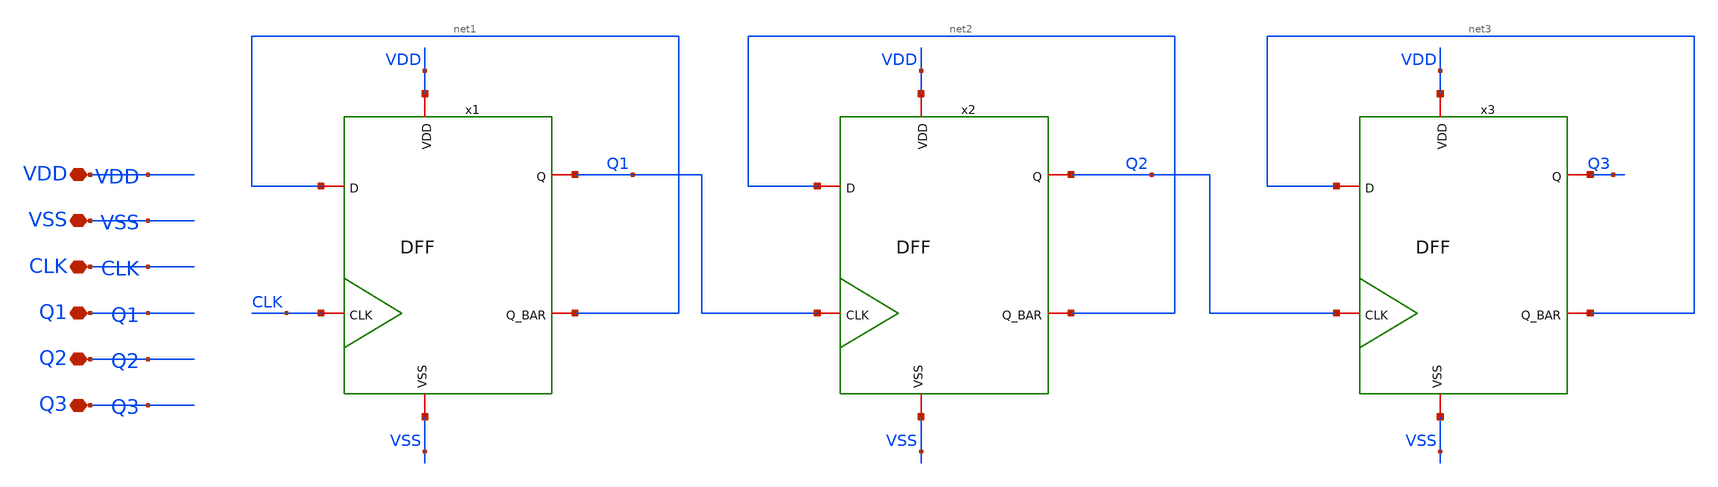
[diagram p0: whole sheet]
** sch_path: designs/libs/xp_core_analog/xp_DIV8/DIVD8.sch
**.subckt DIVD8 VDD VSS CLK Q1 Q2 Q3
*.iopin VDD
*.iopin VSS
*.iopin CLK
*.iopin Q1
*.iopin Q2
*.iopin Q3
x1 VDD VSS CLK net1 Q1 net1 DFF
x2 VDD VSS Q1 net2 Q2 net2 DFF
x3 VDD VSS Q2 net3 Q3 net3 DFF
**.ends

* expanding   symbol:  libs/core_analog/xp_DFF/DFF.sym # of pins=6
** sym_path: designs/libs/core_analog/xp_DFF/DFF.sym
** sch_path: designs/libs/core_analog/xp_DFF/DFF.sch
.subckt DFF VDD VSS CLK D Q Q_BAR
*.iopin VDD
*.iopin VSS
*.iopin CLK
*.iopin D
*.iopin Q_BAR
*.iopin Q
XM1 CLK_B CLK VSS VSS nfet_03v3 L=0.28u W=0.5u nf=1 ad='int((nf+1)/2) * W/nf * 0.18u' as='int((nf+2)/2) * W/nf * 0.18u'
+ pd='2*int((nf+1)/2) * (W/nf + 0.18u)' ps='2*int((nf+2)/2) * (W/nf + 0.18u)' nrd='0.18u / W' nrs='0.18u / W'
+ sa=0 sb=0 sd=0 m=1
XM2 CLK_B CLK VDD VDD pfet_03v3 L=0.28u W=1u nf=1 ad='int((nf+1)/2) * W/nf * 0.18u' as='int((nf+2)/2) * W/nf * 0.18u'
+ pd='2*int((nf+1)/2) * (W/nf + 0.18u)' ps='2*int((nf+2)/2) * (W/nf + 0.18u)' nrd='0.18u / W' nrs='0.18u / W'
+ sa=0 sb=0 sd=0 m=1
XM3 net1 D net3 VSS nfet_03v3 L=0.28u W=0.5u nf=1 ad='int((nf+1)/2) * W/nf * 0.18u' as='int((nf+2)/2) * W/nf * 0.18u'
+ pd='2*int((nf+1)/2) * (W/nf + 0.18u)' ps='2*int((nf+2)/2) * (W/nf + 0.18u)' nrd='0.18u / W' nrs='0.18u / W'
+ sa=0 sb=0 sd=0 m=1
XM4 net1 D net2 VDD pfet_03v3 L=0.28u W=1u nf=1 ad='int((nf+1)/2) * W/nf * 0.18u' as='int((nf+2)/2) * W/nf * 0.18u'
+ pd='2*int((nf+1)/2) * (W/nf + 0.18u)' ps='2*int((nf+2)/2) * (W/nf + 0.18u)' nrd='0.18u / W' nrs='0.18u / W'
+ sa=0 sb=0 sd=0 m=1
XM5 net2 CLK VDD VDD pfet_03v3 L=0.28u W=1u nf=1 ad='int((nf+1)/2) * W/nf * 0.18u' as='int((nf+2)/2) * W/nf * 0.18u'
+ pd='2*int((nf+1)/2) * (W/nf + 0.18u)' ps='2*int((nf+2)/2) * (W/nf + 0.18u)' nrd='0.18u / W' nrs='0.18u / W'
+ sa=0 sb=0 sd=0 m=1
XM6 net3 CLK_B VSS VSS nfet_03v3 L=0.28u W=0.5u nf=1 ad='int((nf+1)/2) * W/nf * 0.18u' as='int((nf+2)/2) * W/nf * 0.18u'
+ pd='2*int((nf+1)/2) * (W/nf + 0.18u)' ps='2*int((nf+2)/2) * (W/nf + 0.18u)' nrd='0.18u / W' nrs='0.18u / W'
+ sa=0 sb=0 sd=0 m=1
XM7 net1 CLK_B net6 VSS nfet_03v3 L=0.28u W=0.22u nf=1 ad='int((nf+1)/2) * W/nf * 0.18u' as='int((nf+2)/2) * W/nf * 0.18u'
+ pd='2*int((nf+1)/2) * (W/nf + 0.18u)' ps='2*int((nf+2)/2) * (W/nf + 0.18u)' nrd='0.18u / W' nrs='0.18u / W'
+ sa=0 sb=0 sd=0 m=1
XM8 net1 CLK net4 VDD pfet_03v3 L=0.28u W=1u nf=1 ad='int((nf+1)/2) * W/nf * 0.18u' as='int((nf+2)/2) * W/nf * 0.18u'
+ pd='2*int((nf+1)/2) * (W/nf + 0.18u)' ps='2*int((nf+2)/2) * (W/nf + 0.18u)' nrd='0.18u / W' nrs='0.18u / W'
+ sa=0 sb=0 sd=0 m=1
XM9 net4 net5 VDD VDD pfet_03v3 L=0.28u W=1u nf=1 ad='int((nf+1)/2) * W/nf * 0.18u' as='int((nf+2)/2) * W/nf * 0.18u'
+ pd='2*int((nf+1)/2) * (W/nf + 0.18u)' ps='2*int((nf+2)/2) * (W/nf + 0.18u)' nrd='0.18u / W' nrs='0.18u / W'
+ sa=0 sb=0 sd=0 m=1
XM10 net6 net5 VSS VSS nfet_03v3 L=0.28u W=0.22u nf=1 ad='int((nf+1)/2) * W/nf * 0.18u' as='int((nf+2)/2) * W/nf * 0.18u'
+ pd='2*int((nf+1)/2) * (W/nf + 0.18u)' ps='2*int((nf+2)/2) * (W/nf + 0.18u)' nrd='0.18u / W' nrs='0.18u / W'
+ sa=0 sb=0 sd=0 m=1
XM11 net5 net1 VSS VSS nfet_03v3 L=0.28u W=0.5u nf=1 ad='int((nf+1)/2) * W/nf * 0.18u' as='int((nf+2)/2) * W/nf * 0.18u'
+ pd='2*int((nf+1)/2) * (W/nf + 0.18u)' ps='2*int((nf+2)/2) * (W/nf + 0.18u)' nrd='0.18u / W' nrs='0.18u / W'
+ sa=0 sb=0 sd=0 m=1
XM12 net5 net1 VDD VDD pfet_03v3 L=0.28u W=1u nf=1 ad='int((nf+1)/2) * W/nf * 0.18u' as='int((nf+2)/2) * W/nf * 0.18u'
+ pd='2*int((nf+1)/2) * (W/nf + 0.18u)' ps='2*int((nf+2)/2) * (W/nf + 0.18u)' nrd='0.18u / W' nrs='0.18u / W'
+ sa=0 sb=0 sd=0 m=1
XM13 net7 CLK net9 VSS nfet_03v3 L=0.28u W=0.5u nf=1 ad='int((nf+1)/2) * W/nf * 0.18u' as='int((nf+2)/2) * W/nf * 0.18u'
+ pd='2*int((nf+1)/2) * (W/nf + 0.18u)' ps='2*int((nf+2)/2) * (W/nf + 0.18u)' nrd='0.18u / W' nrs='0.18u / W'
+ sa=0 sb=0 sd=0 m=1
XM14 net7 CLK_B net8 VDD pfet_03v3 L=0.28u W=1u nf=1 ad='int((nf+1)/2) * W/nf * 0.18u' as='int((nf+2)/2) * W/nf * 0.18u'
+ pd='2*int((nf+1)/2) * (W/nf + 0.18u)' ps='2*int((nf+2)/2) * (W/nf + 0.18u)' nrd='0.18u / W' nrs='0.18u / W'
+ sa=0 sb=0 sd=0 m=1
XM15 net8 net5 VDD VDD pfet_03v3 L=0.28u W=1u nf=1 ad='int((nf+1)/2) * W/nf * 0.18u' as='int((nf+2)/2) * W/nf * 0.18u'
+ pd='2*int((nf+1)/2) * (W/nf + 0.18u)' ps='2*int((nf+2)/2) * (W/nf + 0.18u)' nrd='0.18u / W' nrs='0.18u / W'
+ sa=0 sb=0 sd=0 m=1
XM16 net9 net5 VSS VSS nfet_03v3 L=0.28u W=0.5u nf=1 ad='int((nf+1)/2) * W/nf * 0.18u' as='int((nf+2)/2) * W/nf * 0.18u'
+ pd='2*int((nf+1)/2) * (W/nf + 0.18u)' ps='2*int((nf+2)/2) * (W/nf + 0.18u)' nrd='0.18u / W' nrs='0.18u / W'
+ sa=0 sb=0 sd=0 m=1
XM17 net7 CLK net12 VSS nfet_03v3 L=0.28u W=0.22u nf=1 ad='int((nf+1)/2) * W/nf * 0.18u' as='int((nf+2)/2) * W/nf * 0.18u'
+ pd='2*int((nf+1)/2) * (W/nf + 0.18u)' ps='2*int((nf+2)/2) * (W/nf + 0.18u)' nrd='0.18u / W' nrs='0.18u / W'
+ sa=0 sb=0 sd=0 m=1
XM18 net7 CLK_B net10 VDD pfet_03v3 L=0.28u W=1u nf=1 ad='int((nf+1)/2) * W/nf * 0.18u' as='int((nf+2)/2) * W/nf * 0.18u'
+ pd='2*int((nf+1)/2) * (W/nf + 0.18u)' ps='2*int((nf+2)/2) * (W/nf + 0.18u)' nrd='0.18u / W' nrs='0.18u / W'
+ sa=0 sb=0 sd=0 m=1
XM19 net10 net11 VDD VDD pfet_03v3 L=0.28u W=1u nf=1 ad='int((nf+1)/2) * W/nf * 0.18u' as='int((nf+2)/2) * W/nf * 0.18u'
+ pd='2*int((nf+1)/2) * (W/nf + 0.18u)' ps='2*int((nf+2)/2) * (W/nf + 0.18u)' nrd='0.18u / W' nrs='0.18u / W'
+ sa=0 sb=0 sd=0 m=1
XM20 net12 net11 VSS VSS nfet_03v3 L=0.28u W=0.22u nf=1 ad='int((nf+1)/2) * W/nf * 0.18u' as='int((nf+2)/2) * W/nf * 0.18u'
+ pd='2*int((nf+1)/2) * (W/nf + 0.18u)' ps='2*int((nf+2)/2) * (W/nf + 0.18u)' nrd='0.18u / W' nrs='0.18u / W'
+ sa=0 sb=0 sd=0 m=1
XM21 net11 net7 VSS VSS nfet_03v3 L=0.28u W=0.5u nf=2 ad='int((nf+1)/2) * W/nf * 0.18u' as='int((nf+2)/2) * W/nf * 0.18u'
+ pd='2*int((nf+1)/2) * (W/nf + 0.18u)' ps='2*int((nf+2)/2) * (W/nf + 0.18u)' nrd='0.18u / W' nrs='0.18u / W'
+ sa=0 sb=0 sd=0 m=1
XM22 net11 net7 VDD VDD pfet_03v3 L=0.28u W=1u nf=2 ad='int((nf+1)/2) * W/nf * 0.18u' as='int((nf+2)/2) * W/nf * 0.18u'
+ pd='2*int((nf+1)/2) * (W/nf + 0.18u)' ps='2*int((nf+2)/2) * (W/nf + 0.18u)' nrd='0.18u / W' nrs='0.18u / W'
+ sa=0 sb=0 sd=0 m=1
XM23 Q_BAR net11 VSS VSS nfet_03v3 L=0.28u W=0.5u nf=1 ad='int((nf+1)/2) * W/nf * 0.18u' as='int((nf+2)/2) * W/nf * 0.18u'
+ pd='2*int((nf+1)/2) * (W/nf + 0.18u)' ps='2*int((nf+2)/2) * (W/nf + 0.18u)' nrd='0.18u / W' nrs='0.18u / W'
+ sa=0 sb=0 sd=0 m=1
XM24 Q_BAR net11 VDD VDD pfet_03v3 L=0.28u W=1u nf=1 ad='int((nf+1)/2) * W/nf * 0.18u' as='int((nf+2)/2) * W/nf * 0.18u'
+ pd='2*int((nf+1)/2) * (W/nf + 0.18u)' ps='2*int((nf+2)/2) * (W/nf + 0.18u)' nrd='0.18u / W' nrs='0.18u / W'
+ sa=0 sb=0 sd=0 m=1
XM25 Q Q_BAR VSS VSS nfet_03v3 L=0.28u W=0.5u nf=1 ad='int((nf+1)/2) * W/nf * 0.18u' as='int((nf+2)/2) * W/nf * 0.18u'
+ pd='2*int((nf+1)/2) * (W/nf + 0.18u)' ps='2*int((nf+2)/2) * (W/nf + 0.18u)' nrd='0.18u / W' nrs='0.18u / W'
+ sa=0 sb=0 sd=0 m=1
XM26 Q Q_BAR VDD VDD pfet_03v3 L=0.28u W=1u nf=1 ad='int((nf+1)/2) * W/nf * 0.18u' as='int((nf+2)/2) * W/nf * 0.18u'
+ pd='2*int((nf+1)/2) * (W/nf + 0.18u)' ps='2*int((nf+2)/2) * (W/nf + 0.18u)' nrd='0.18u / W' nrs='0.18u / W'
+ sa=0 sb=0 sd=0 m=1
.ends

.end
